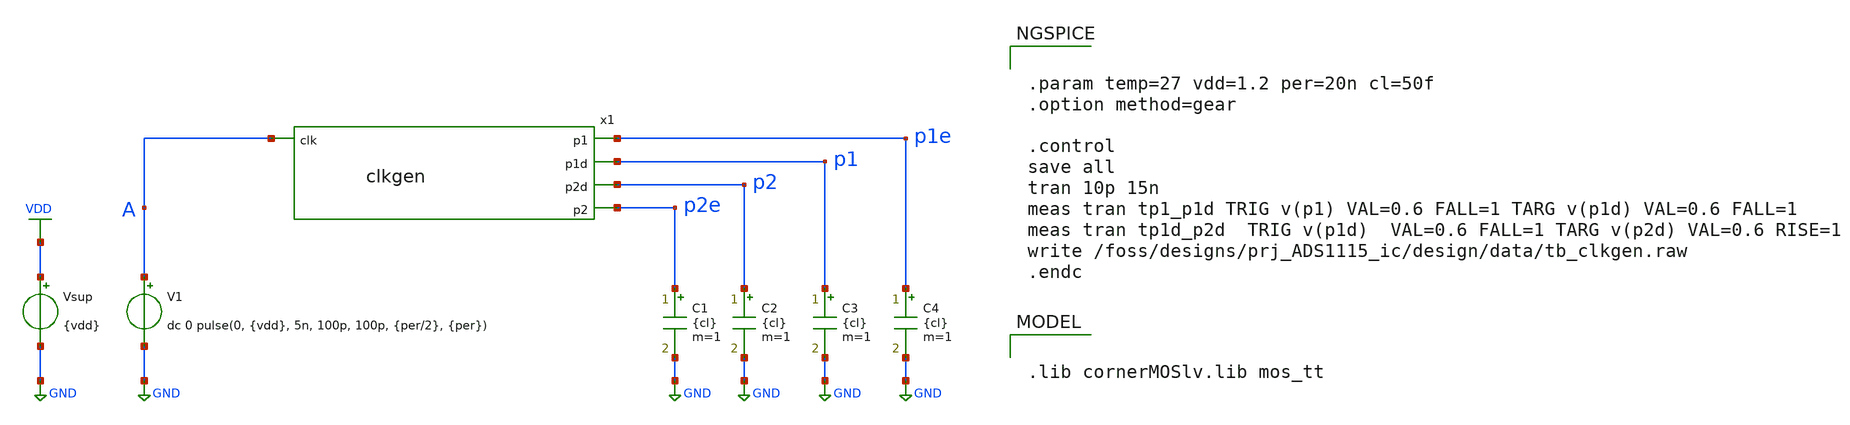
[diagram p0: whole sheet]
** sch_path: design/design_clkgen/tb_clkgen.sch
**.subckt tb_clkgen
V1 A GND dc 0 pulse(0, {vdd}, 5n, 100p, 100p, {per/2}, {per})
Vsup VDD GND {vdd}
x1 p1e p1 A p2 p2e clkgen
C1 p2e GND {cl} m=1
C2 p2 GND {cl} m=1
C3 p1 GND {cl} m=1
C4 p1e GND {cl} m=1
**** begin user architecture code

.lib cornerMOSlv.lib mos_tt



.param temp=27 vdd=1.2 per=20n cl=50f
.option method=gear

.control
save all
tran 10p 15n
meas tran tp1_p1d TRIG v(p1) VAL=0.6 FALL=1 TARG v(p1d) VAL=0.6 FALL=1
meas tran tp1d_p2d  TRIG v(p1d)  VAL=0.6 FALL=1 TARG v(p2d) VAL=0.6 RISE=1
write /foss/designs/prj_ADS1115_ic/design/data/tb_clkgen.raw
.endc


**** end user architecture code
**.ends
.GLOBAL GND
.GLOBAL VDD
.end
